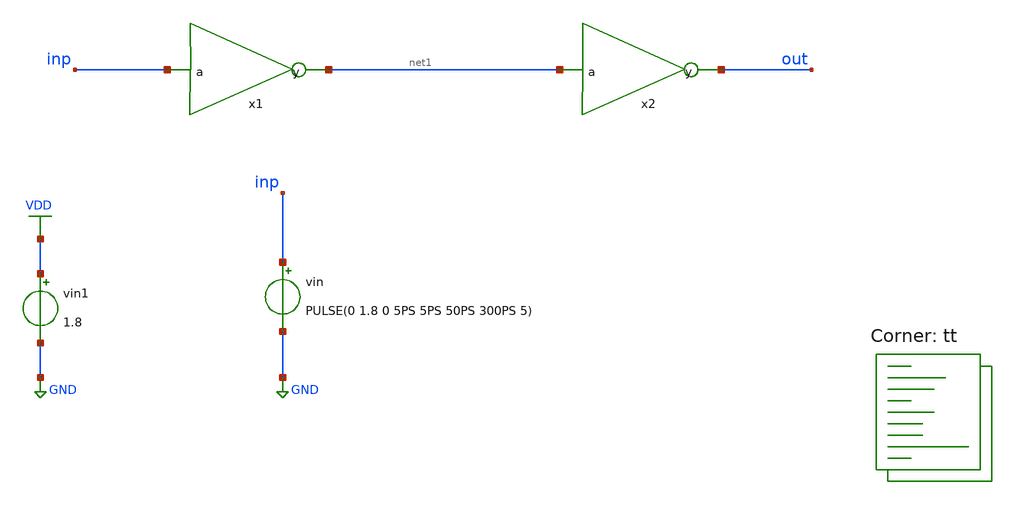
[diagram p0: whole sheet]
** sch_path: assignments/assignment3/assign1a.sch
**.subckt assign1a
vin inp GND PULSE(0 1.8 0 5PS 5PS 50PS 300PS 5)
vin1 VDD GND 1.8
x1 net1 inp inverter
x2 out net1 inverter
**** begin user architecture code


.param width_p = 0.42

.control
* Run 1: Wp = 0.42
alterparam width_p = 0.42
reset
tran 0.1p 250p
let out_042 = v(net1)
let in_042  = v(inp)
meas tran tlh_042 trig v(inp) val=0.9 rise=1 targ v(net1) val=0.9 rise=1
meas tran thl_042 trig v(inp) val=0.9 fall=1 targ v(net1) val=0.9 fall=1
let delay_042 = (tlh_042 + thl_042) / 2
echo Wp = 0.42 : delay = $&delay_042

* Run 2: Wp = 0.84
alterparam width_p = 0.84
reset
tran 0.1p 250p
let out_084 = v(net1)
let in_084  = v(inp)
meas tran tlh_084 trig v(inp) val=0.9 rise=1 targ v(net1) val=0.9 rise=1
meas tran thl_084 trig v(inp) val=0.9 fall=1 targ v(net1) val=0.9 fall=1
let delay_084 = (tlh_084 + thl_084) / 2
echo Wp = 0.84 : delay = $&delay_084

* Run 3: Wp = 1.26
alterparam width_p = 1.26
reset
tran 0.1p 250p
let out_126 = v(net1)
let in_126  = v(inp)
meas tran tlh_126 trig v(inp) val=0.9 rise=1 targ v(net1) val=0.9 rise=1
meas tran thl_126 trig v(inp) val=0.9 fall=1 targ v(net1) val=0.9 fall=1
let delay_126 = (tlh_126 + thl_126) / 2
echo Wp = 1.26 : delay = $&delay_126

* Overlay all three runs on one plot, each curve tagged by its Wp
plot tran1.out_042 tran2.out_084 tran3.out_126 tran1.in_042 xlabel Time ylabel Voltage title 'v(out) for Wp = 0.42 / 0.84 / 1.26'
.endc


.lib $::SKYWATER_MODELS/sky130.lib.spice tt
**** end user architecture code
**.ends

* expanding   symbol:  inverter.sym # of pins=2
** sym_path: assignments/assignment3/inverter.sym
** sch_path: assignments/assignment3/inverter.sch
.subckt inverter y a
*.ipin a
*.opin y
XM1 y a GND GND sky130_fd_pr__nfet_01v8 L=0.15 W=0.42 nf=1 ad='int((nf+1)/2) * W/nf * 0.29' as='int((nf+2)/2) * W/nf * 0.29'
+ pd='2*int((nf+1)/2) * (W/nf + 0.29)' ps='2*int((nf+2)/2) * (W/nf + 0.29)' nrd='0.29 / W' nrs='0.29 / W'
+ sa=0 sb=0 sd=0 mult=1 m=1
XM2 y a VDD VDD sky130_fd_pr__pfet_01v8 L=0.15 W={width_p} nf=1 ad='int((nf+1)/2) * W/nf * 0.29' as='int((nf+2)/2) * W/nf * 0.29'
+ pd='2*int((nf+1)/2) * (W/nf + 0.29)' ps='2*int((nf+2)/2) * (W/nf + 0.29)' nrd='0.29 / W' nrs='0.29 / W'
+ sa=0 sb=0 sd=0 mult=1 m=1
.ends

.GLOBAL GND
.GLOBAL VDD
.end
